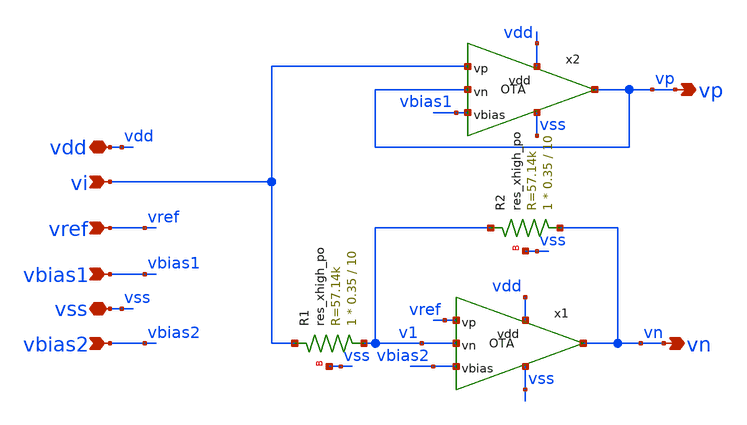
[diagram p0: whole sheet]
** sch_path: xschem/src/S_to_D/S_to_D.sch
**.subckt S_to_D vdd vss vi vp vn vref vbias1 vbias2
*.iopin vdd
*.iopin vss
*.ipin vi
*.opin vp
*.opin vn
*.ipin vref
*.ipin vbias1
*.ipin vbias2
x1 vdd vref v1 vbias2 vss vn OTA
XR2 vn v1 vss sky130_fd_pr__res_xhigh_po L=10 mult=1 m=1
x2 vdd vi vp vbias1 vss vp OTA
XR1 v1 vi vss sky130_fd_pr__res_xhigh_po L=10 mult=1 m=1
**.ends

* expanding   symbol:  src/OTA/OTA.sym # of pins=6
** sym_path: xschem/src/OTA/OTA.sym
** sch_path: xschem/src/OTA/OTA.sch
.subckt OTA vdd vp vn vbias vss vout
*.ipin vp
*.ipin vn
*.ipin vbias
*.iopin vss
*.iopin vdd
*.opin vout
XM1 v1 vp vc vc sky130_fd_pr__pfet_01v8_lvt L=1 W=4 nf=1 ad='int((nf+1)/2) * W/nf * 0.29' as='int((nf+2)/2) * W/nf * 0.29'
+ pd='2*int((nf+1)/2) * (W/nf + 0.29)' ps='2*int((nf+2)/2) * (W/nf + 0.29)' nrd='0.29 / W' nrs='0.29 / W'
+ sa=0 sb=0 sd=0 mult=16 m=16
XM2 vf vn vc vc sky130_fd_pr__pfet_01v8_lvt L=1 W=4 nf=1 ad='int((nf+1)/2) * W/nf * 0.29' as='int((nf+2)/2) * W/nf * 0.29'
+ pd='2*int((nf+1)/2) * (W/nf + 0.29)' ps='2*int((nf+2)/2) * (W/nf + 0.29)' nrd='0.29 / W' nrs='0.29 / W'
+ sa=0 sb=0 sd=0 mult=16 m=16
XM3 vc vbias vdd vdd sky130_fd_pr__pfet_01v8_lvt L=1 W=2 nf=2 ad='int((nf+1)/2) * W/nf * 0.29' as='int((nf+2)/2) * W/nf * 0.29'
+ pd='2*int((nf+1)/2) * (W/nf + 0.29)' ps='2*int((nf+2)/2) * (W/nf + 0.29)' nrd='0.29 / W' nrs='0.29 / W'
+ sa=0 sb=0 sd=0 mult=24 m=24
XM4 v1 vf vss vss sky130_fd_pr__nfet_01v8_lvt L=1 W=1 nf=1 ad='int((nf+1)/2) * W/nf * 0.29' as='int((nf+2)/2) * W/nf * 0.29'
+ pd='2*int((nf+1)/2) * (W/nf + 0.29)' ps='2*int((nf+2)/2) * (W/nf + 0.29)' nrd='0.29 / W' nrs='0.29 / W'
+ sa=0 sb=0 sd=0 mult=16 m=16
XM5 vf vf vss vss sky130_fd_pr__nfet_01v8_lvt L=1 W=1 nf=1 ad='int((nf+1)/2) * W/nf * 0.29' as='int((nf+2)/2) * W/nf * 0.29'
+ pd='2*int((nf+1)/2) * (W/nf + 0.29)' ps='2*int((nf+2)/2) * (W/nf + 0.29)' nrd='0.29 / W' nrs='0.29 / W'
+ sa=0 sb=0 sd=0 mult=16 m=16
XM6 vbias vbias vdd vdd sky130_fd_pr__pfet_01v8_lvt L=1 W=2 nf=2 ad='int((nf+1)/2) * W/nf * 0.29' as='int((nf+2)/2) * W/nf * 0.29'
+ pd='2*int((nf+1)/2) * (W/nf + 0.29)' ps='2*int((nf+2)/2) * (W/nf + 0.29)' nrd='0.29 / W' nrs='0.29 / W'
+ sa=0 sb=0 sd=0 mult=24 m=24
XM7 vout vbias vdd vdd sky130_fd_pr__pfet_01v8_lvt L=1 W=2 nf=2 ad='int((nf+1)/2) * W/nf * 0.29' as='int((nf+2)/2) * W/nf * 0.29'
+ pd='2*int((nf+1)/2) * (W/nf + 0.29)' ps='2*int((nf+2)/2) * (W/nf + 0.29)' nrd='0.29 / W' nrs='0.29 / W'
+ sa=0 sb=0 sd=0 mult=48 m=48
XM8 vout v1 vss vss sky130_fd_pr__nfet_01v8_lvt L=1 W=1 nf=1 ad='int((nf+1)/2) * W/nf * 0.29' as='int((nf+2)/2) * W/nf * 0.29'
+ pd='2*int((nf+1)/2) * (W/nf + 0.29)' ps='2*int((nf+2)/2) * (W/nf + 0.29)' nrd='0.29 / W' nrs='0.29 / W'
+ sa=0 sb=0 sd=0 mult=64 m=64
XR1 v1 net1 vss sky130_fd_pr__res_xhigh_po W=0.35 L=0.5 mult=1 m=1
XC2 net1 vout sky130_fd_pr__cap_mim_m3_1 W=14 L=14 MF=1 m=1
.ends

.end
